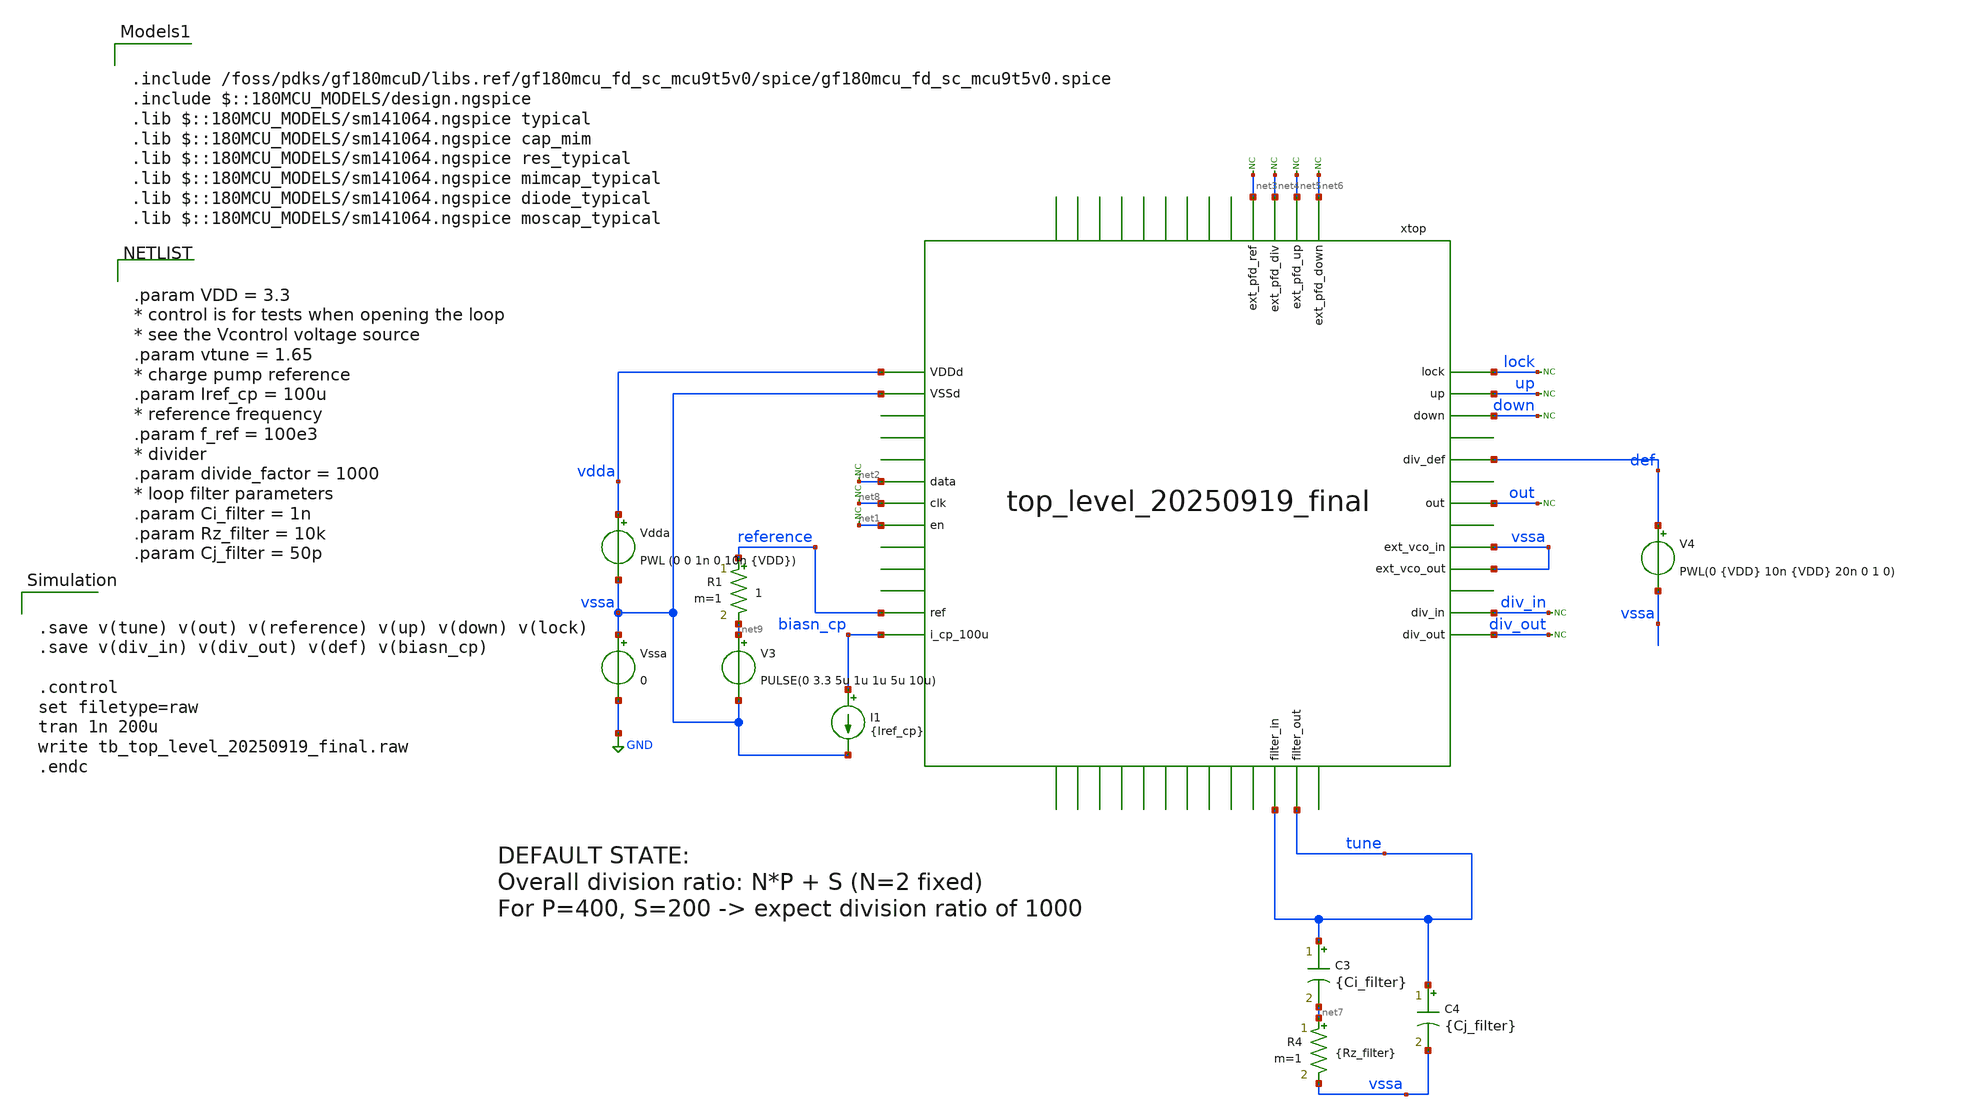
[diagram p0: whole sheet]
** sch_path: designs/libs/tb_top_level/tb_top_level_20250919_final.sch
**.subckt tb_top_level_20250919_final
Vssa vssa GND 0
Vdda vdda vssa PWL (0 0 1n 0 10n {VDD})
V4 def vssa PWL(0 {VDD} 10n {VDD} 20n 0 1 0)
* noconn #net3
* noconn #net4
* noconn #net5
* noconn #net6
* noconn div_in
* noconn div_out
* noconn down
* noconn up
* noconn lock
C3 tune net7 {Ci_filter} m=1
R4 net7 vssa {Rz_filter} m=1
C4 tune vssa {Cj_filter} m=1
* noconn out
V3 net9 vssa PULSE(0 3.3 5u 1u 1u 5u 10u)
R1 reference net9 1 m=1
I1 biasn_cp vssa {Iref_cp}
* noconn #net2
* noconn #net8
* noconn #net1
xtop vdda vssa net2 net8 net1 reference biasn_cp net3 net4 net5 net6 lock up down tune vssa div_in
+ div_out out tune vssa def top_level_20250919_final
**** begin user architecture code


.param VDD = 3.3
* control is for tests when opening the loop
* see the Vcontrol voltage source
.param vtune = 1.65
* charge pump reference
.param Iref_cp = 100u
* reference frequency
.param f_ref = 100e3
* divider
.param divide_factor = 1000
* loop filter parameters
.param Ci_filter = 1n
.param Rz_filter = 10k
.param Cj_filter = 50p



.include /foss/pdks/gf180mcuD/libs.ref/gf180mcu_fd_sc_mcu9t5v0/spice/gf180mcu_fd_sc_mcu9t5v0.spice
.include $::180MCU_MODELS/design.ngspice
.lib $::180MCU_MODELS/sm141064.ngspice typical
.lib $::180MCU_MODELS/sm141064.ngspice cap_mim
.lib $::180MCU_MODELS/sm141064.ngspice res_typical
.lib $::180MCU_MODELS/sm141064.ngspice mimcap_typical
.lib $::180MCU_MODELS/sm141064.ngspice diode_typical
.lib $::180MCU_MODELS/sm141064.ngspice moscap_typical



.save v(tune) v(out) v(reference) v(up) v(down) v(lock)
.save v(div_in) v(div_out) v(def) v(biasn_cp)

.control
set filetype=raw
tran 1n 200u
write tb_top_level_20250919_final.raw
.endc


**** end user architecture code
**.ends
.GLOBAL GND
.end
